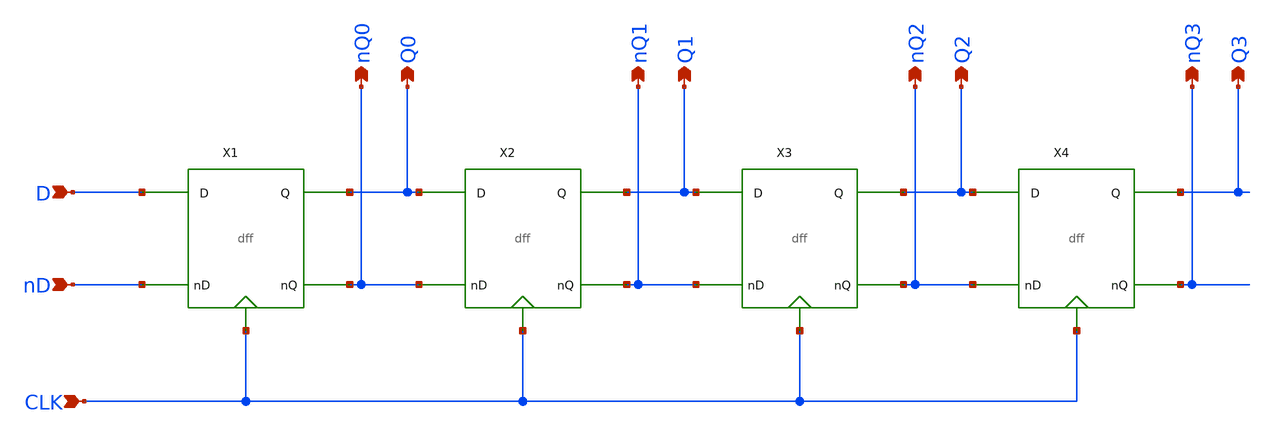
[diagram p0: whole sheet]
** sch_path: mini2/schem/shiftreg_4_lvs.sch
**.subckt shiftreg_4_lvs nQ0 Q0 nQ1 Q1 nQ2 Q2 nQ3 Q3 CLK D nD
*.opin nQ0
*.opin Q0
*.opin nQ1
*.opin Q1
*.opin nQ2
*.opin Q2
*.opin nQ3
*.opin Q3
*.ipin CLK
*.ipin D
*.ipin nD
X1 D nD CLK nQ0 Q0 dff
X2 Q0 nQ0 CLK nQ1 Q1 dff
X3 Q1 nQ1 CLK nQ2 Q2 dff
X4 Q2 nQ2 CLK nQ3 Q3 dff
**.ends

* expanding   symbol:  /home/madvlsi/MADVLSI/mini2/schem/dff.sym # of pins=5
** sym_path: mini2/schem/dff.sym
** sch_path: mini2/schem/dff.sch
.subckt dff D nD CLK nQ Q
*.ipin nD
*.ipin D
*.iopin CLK
*.opin nQ
*.opin Q
XM1 net3 CLK GND GND sky130_fd_pr__nfet_01v8 L=0.15 W=1 nf=1 ad='int((nf+1)/2) * W/nf * 0.29' as='int((nf+2)/2) * W/nf * 0.29'
+ pd='2*int((nf+1)/2) * (W/nf + 0.29)' ps='2*int((nf+2)/2) * (W/nf + 0.29)' nrd='0.29 / W' nrs='0.29 / W'
+ sa=0 sb=0 sd=0 mult=1 m=1
XM2 net4 CLK GND GND sky130_fd_pr__nfet_01v8 L=0.15 W=1 nf=1 ad='int((nf+1)/2) * W/nf * 0.29' as='int((nf+2)/2) * W/nf * 0.29'
+ pd='2*int((nf+1)/2) * (W/nf + 0.29)' ps='2*int((nf+2)/2) * (W/nf + 0.29)' nrd='0.29 / W' nrs='0.29 / W'
+ sa=0 sb=0 sd=0 mult=1 m=1
XM3 net2 net1 net3 GND sky130_fd_pr__nfet_01v8 L=0.15 W=1 nf=1 ad='int((nf+1)/2) * W/nf * 0.29' as='int((nf+2)/2) * W/nf * 0.29'
+ pd='2*int((nf+1)/2) * (W/nf + 0.29)' ps='2*int((nf+2)/2) * (W/nf + 0.29)' nrd='0.29 / W' nrs='0.29 / W'
+ sa=0 sb=0 sd=0 mult=1 m=1
XM4 net1 net2 net4 GND sky130_fd_pr__nfet_01v8 L=0.15 W=1 nf=1 ad='int((nf+1)/2) * W/nf * 0.29' as='int((nf+2)/2) * W/nf * 0.29'
+ pd='2*int((nf+1)/2) * (W/nf + 0.29)' ps='2*int((nf+2)/2) * (W/nf + 0.29)' nrd='0.29 / W' nrs='0.29 / W'
+ sa=0 sb=0 sd=0 mult=1 m=1
XM5 net2 CLK D VDD sky130_fd_pr__pfet_01v8 L=0.15 W=1 nf=1 ad='int((nf+1)/2) * W/nf * 0.29' as='int((nf+2)/2) * W/nf * 0.29'
+ pd='2*int((nf+1)/2) * (W/nf + 0.29)' ps='2*int((nf+2)/2) * (W/nf + 0.29)' nrd='0.29 / W' nrs='0.29 / W'
+ sa=0 sb=0 sd=0 mult=1 m=1
XM6 VDD net1 net2 VDD sky130_fd_pr__pfet_01v8 L=0.15 W=1 nf=1 ad='int((nf+1)/2) * W/nf * 0.29' as='int((nf+2)/2) * W/nf * 0.29'
+ pd='2*int((nf+1)/2) * (W/nf + 0.29)' ps='2*int((nf+2)/2) * (W/nf + 0.29)' nrd='0.29 / W' nrs='0.29 / W'
+ sa=0 sb=0 sd=0 mult=1 m=1
XM7 net1 CLK nD VDD sky130_fd_pr__pfet_01v8 L=0.15 W=1 nf=1 ad='int((nf+1)/2) * W/nf * 0.29' as='int((nf+2)/2) * W/nf * 0.29'
+ pd='2*int((nf+1)/2) * (W/nf + 0.29)' ps='2*int((nf+2)/2) * (W/nf + 0.29)' nrd='0.29 / W' nrs='0.29 / W'
+ sa=0 sb=0 sd=0 mult=1 m=1
XM8 VDD net2 net1 VDD sky130_fd_pr__pfet_01v8 L=0.15 W=1 nf=1 ad='int((nf+1)/2) * W/nf * 0.29' as='int((nf+2)/2) * W/nf * 0.29'
+ pd='2*int((nf+1)/2) * (W/nf + 0.29)' ps='2*int((nf+2)/2) * (W/nf + 0.29)' nrd='0.29 / W' nrs='0.29 / W'
+ sa=0 sb=0 sd=0 mult=1 m=1
XM9 Q CLK net2 GND sky130_fd_pr__nfet_01v8 L=0.15 W=1 nf=1 ad='int((nf+1)/2) * W/nf * 0.29' as='int((nf+2)/2) * W/nf * 0.29'
+ pd='2*int((nf+1)/2) * (W/nf + 0.29)' ps='2*int((nf+2)/2) * (W/nf + 0.29)' nrd='0.29 / W' nrs='0.29 / W'
+ sa=0 sb=0 sd=0 mult=1 m=1
XM10 nQ CLK net1 GND sky130_fd_pr__nfet_01v8 L=0.15 W=1 nf=1 ad='int((nf+1)/2) * W/nf * 0.29' as='int((nf+2)/2) * W/nf * 0.29'
+ pd='2*int((nf+1)/2) * (W/nf + 0.29)' ps='2*int((nf+2)/2) * (W/nf + 0.29)' nrd='0.29 / W' nrs='0.29 / W'
+ sa=0 sb=0 sd=0 mult=1 m=1
XM11 GND nQ Q GND sky130_fd_pr__nfet_01v8 L=0.15 W=1 nf=1 ad='int((nf+1)/2) * W/nf * 0.29' as='int((nf+2)/2) * W/nf * 0.29'
+ pd='2*int((nf+1)/2) * (W/nf + 0.29)' ps='2*int((nf+2)/2) * (W/nf + 0.29)' nrd='0.29 / W' nrs='0.29 / W'
+ sa=0 sb=0 sd=0 mult=1 m=1
XM12 GND Q nQ GND sky130_fd_pr__nfet_01v8 L=0.15 W=1 nf=1 ad='int((nf+1)/2) * W/nf * 0.29' as='int((nf+2)/2) * W/nf * 0.29'
+ pd='2*int((nf+1)/2) * (W/nf + 0.29)' ps='2*int((nf+2)/2) * (W/nf + 0.29)' nrd='0.29 / W' nrs='0.29 / W'
+ sa=0 sb=0 sd=0 mult=1 m=1
XM13 net6 CLK VDD VDD sky130_fd_pr__pfet_01v8 L=0.15 W=1 nf=1 ad='int((nf+1)/2) * W/nf * 0.29' as='int((nf+2)/2) * W/nf * 0.29'
+ pd='2*int((nf+1)/2) * (W/nf + 0.29)' ps='2*int((nf+2)/2) * (W/nf + 0.29)' nrd='0.29 / W' nrs='0.29 / W'
+ sa=0 sb=0 sd=0 mult=1 m=1
XM14 Q nQ net6 VDD sky130_fd_pr__pfet_01v8 L=0.15 W=1 nf=1 ad='int((nf+1)/2) * W/nf * 0.29' as='int((nf+2)/2) * W/nf * 0.29'
+ pd='2*int((nf+1)/2) * (W/nf + 0.29)' ps='2*int((nf+2)/2) * (W/nf + 0.29)' nrd='0.29 / W' nrs='0.29 / W'
+ sa=0 sb=0 sd=0 mult=1 m=1
XM15 net5 CLK VDD VDD sky130_fd_pr__pfet_01v8 L=0.15 W=1 nf=1 ad='int((nf+1)/2) * W/nf * 0.29' as='int((nf+2)/2) * W/nf * 0.29'
+ pd='2*int((nf+1)/2) * (W/nf + 0.29)' ps='2*int((nf+2)/2) * (W/nf + 0.29)' nrd='0.29 / W' nrs='0.29 / W'
+ sa=0 sb=0 sd=0 mult=1 m=1
XM16 nQ Q net5 VDD sky130_fd_pr__pfet_01v8 L=0.15 W=1 nf=1 ad='int((nf+1)/2) * W/nf * 0.29' as='int((nf+2)/2) * W/nf * 0.29'
+ pd='2*int((nf+1)/2) * (W/nf + 0.29)' ps='2*int((nf+2)/2) * (W/nf + 0.29)' nrd='0.29 / W' nrs='0.29 / W'
+ sa=0 sb=0 sd=0 mult=1 m=1
.ends

.GLOBAL VDD
.GLOBAL GND
.end
